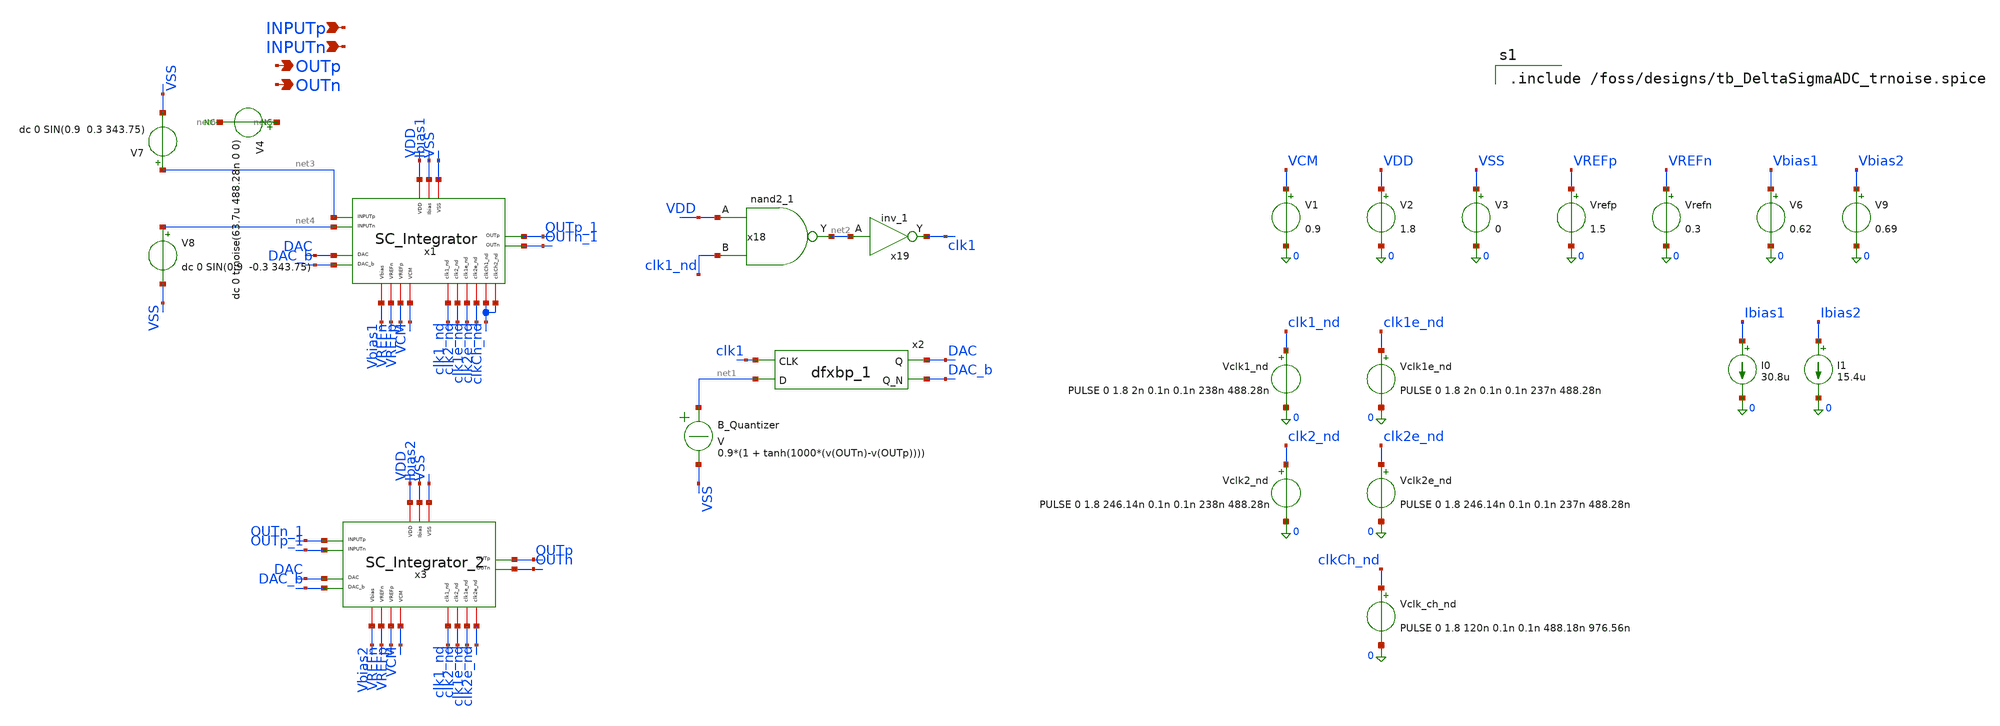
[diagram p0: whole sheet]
** sch_path: xschem/top/DeltaSigmaADC_L2.sch
**.subckt DeltaSigmaADC_L2 OUTp OUTn INPUTp INPUTn
*.opin OUTp
*.opin OUTn
*.ipin INPUTp
*.ipin INPUTn
x1 clkCh_nd VDD clk1_nd OUTp_1 net3 VSS clk2_nd net4 OUTn_1 Ibias1 DAC clk1e_nd VCM DAC_b clk2e_nd
+ VREFp VREFn Vbias1 clkCh_nd SC_Integrator
V1 VCM 0 0.9
V2 VDD 0 1.8
I0 Ibias1 0 30.8u
V3 VSS 0 0
Vrefp VREFp 0 1.5
Vrefn VREFn 0 0.3
V6 Vbias1 0 0.62
Vclk1_nd clk1_nd 0 PULSE 0 1.8 2n 0.1n 0.1n 238n 488.28n
Vclk1e_nd clk1e_nd 0 PULSE 0 1.8 2n 0.1n 0.1n 237n 488.28n
Vclk2_nd clk2_nd 0 PULSE 0 1.8 246.14n 0.1n 0.1n 238n 488.28n
Vclk2e_nd clk2e_nd 0 PULSE 0 1.8 246.14n 0.1n 0.1n 237n 488.28n
B_Quantizer net1 VSS V = 0.9*(1 + tanh(1000*(v(OUTn)-v(OUTp))))
x2 clk1 net1 VSS VSS VDD VDD DAC DAC_b sky130_fd_sc_hd__dfxbp_1
x18 VDD clk1_nd VSS VSS VDD VDD net2 sky130_fd_sc_hd__nand2_1
x19 net2 VSS VSS VDD VDD clk1 sky130_fd_sc_hd__inv_1
x3 VDD clk1_nd OUTp OUTn_1 VSS clk2_nd OUTp_1 OUTn Ibias2 DAC clk1e_nd VCM DAC_b clk2e_nd VREFp
+ VREFn Vbias2 SC_Integrator_2
I1 Ibias2 0 15.4u
Vclk_ch_nd clkCh_nd 0 PULSE 0 1.8 120n 0.1n 0.1n 488.18n 976.56n
V4 net5 net6 dc 0 trnoise(63.7u 488.28n 0 0)
V7 net3 VSS dc 0 SIN(0.9 0.3 343.75)
V8 net4 VSS dc 0 SIN(0.9 -0.3 343.75)
V9 Vbias2 0 0.69
* noconn #net6
* noconn #net5
**** begin user architecture code

.include /foss/designs/tb_DeltaSigmaADC_trnoise.spice

**** end user architecture code
**.ends
.end
